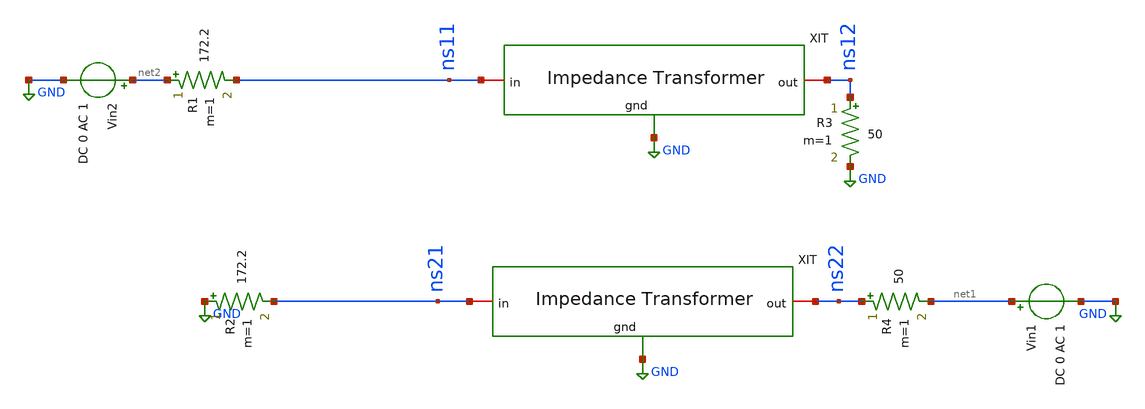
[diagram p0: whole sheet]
** sch_path: impedance-transformer/xschem/impedance-transformer_tb-ac.sch
**.subckt impedance-transformer_tb-ac
Vin1 net1 GND DC 0 AC 1
R3 ns12 GND 50 m=1
R4 ns22 net1 50 m=1
x1 ns11 ns12 GND impedance-transformer
x2 ns21 ns22 GND impedance-transformer
R1 net2 ns11 172.2 m=1
R2 GND ns21 172.2 m=1
Vin2 net2 GND DC 0 AC 1
**** begin user architecture code



.ac lin 1MEG 1.5G 4G
.control
destroy all
set units=degrees
run

set color0=white
set color1=black

let z0=50
let zl=169

* Find two S parameters from test circuit
let s11 = v(ns11)
let s12 = v(ns12)
let s21 = v(ns21)
let s22 = v(ns22)

* Extract Y parameters
*let StoYDelS = ((1+s11)*(1+s22)-s12*s21)*z0
*let y11 = ((1+s22)*(1-s11)+s12*s21/StoYDelS
*let y12=-2*s12/StoYDelS
*let y21=-2*s21/StoYDelS
*let y22 = ((1+s11)*(1-s22)+s12+s21)/StoYDelS

* Extract Z parameters
let StoZDelS = ((1-s11)*(1-s22)-s12*s21)/z0
let z11 = ((1+s11)*(1-s22)+s12*s21)/StoZDelS
let z12 = 2*s12/StoZDelS
let z21 = 2*s21/StoZDelS
let z22=((1-s11)*(1+s22)+s12*s21)/StoZDelS

*plot z11
*plot z12
*plot z21
*plot z22 xlimit 2.4G 2.5G
*plot ph(z22) xlimit 2.4G 2.5G
*plot z22
*plot smith z22
let z_in =z11-z12*z21/(z22+z0)
plot ph(z_in)
plot mag(z_in)
let z_output=z22-(z12*z21/(z11+zl))
plot ph(z_output)
plot mag(z_output)
let gamma=(mag(z_output)-mag(z_in))/(mag(z_output)+mag(z_in))
plot gamma*100
.endc


.lib /home/hugodg/sky130_workspace/skywater-pdk/libraries/sky130_fd_pr_ngspice/latest/models/sky130.lib.spice tt

**** end user architecture code
**.ends

* expanding   symbol:
*+  /home/hugodg/projects_sky130/temp_sensor/impedance-transformer/xschem/impedance-transformer.sym # of pins=3
** sym_path: impedance-transformer/xschem/impedance-transformer.sym
** sch_path: impedance-transformer/xschem/impedance-transformer.sch
.subckt impedance-transformer in out gnd
*.iopin gnd
*.iopin in
*.iopin out
XC0 in gnd sky130_fd_pr__cap_mim_m3_2 W=24.43 L=24.43 MF=9 m=9
XC1 out gnd sky130_fd_pr__cap_mim_m3_2 W=24.962 L=24.962 MF=16 m=16
x1 in out l1
.ends


* expanding   symbol:  /home/hugodg/projects_sky130/temp_sensor/impedance-transformer/xschem/l1.sym
*+ # of pins=2
** sym_path: impedance-transformer/xschem/l1.sym
** sch_path: impedance-transformer/xschem/l1.sch
.subckt l1 p1 p2
*.iopin p2
*.iopin p1
L0 p1 net3 592.7p m=1
Cs1 p1 net1 26.83f m=1
Cs2 p2 net2 24.25f m=1
Rs1 net1 GND 65.02 m=1
Rs2 net2 GND 14.4 m=1
R1 p2 net3 2.935 m=1
.ends

.GLOBAL GND
.end
